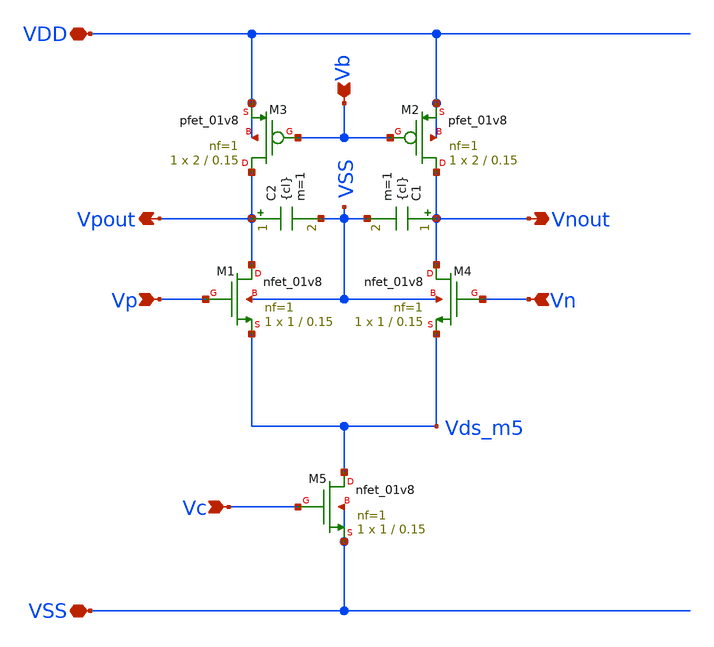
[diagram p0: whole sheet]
** sch_path: xschem/vco_stage_1.sch
**.subckt vco_stage_1 VDD VSS Vp Vn Vb Vc Vpout Vnout
*.iopin VDD
*.iopin VSS
*.ipin Vp
*.ipin Vn
*.ipin Vb
*.ipin Vc
*.opin Vpout
*.opin Vnout
XM1 Vpout Vp Vds_m5 VSS sky130_fd_pr__nfet_01v8 L=0.15 W=1 nf=1 ad='int((nf+1)/2) * W/nf * 0.29' as='int((nf+2)/2) * W/nf * 0.29'
+ pd='2*int((nf+1)/2) * (W/nf + 0.29)' ps='2*int((nf+2)/2) * (W/nf + 0.29)' nrd='0.29 / W' nrs='0.29 / W'
+ sa=0 sb=0 sd=0 mult=1 m=1
XM4 Vnout Vn Vds_m5 VSS sky130_fd_pr__nfet_01v8 L=0.15 W=1 nf=1 ad='int((nf+1)/2) * W/nf * 0.29' as='int((nf+2)/2) * W/nf * 0.29'
+ pd='2*int((nf+1)/2) * (W/nf + 0.29)' ps='2*int((nf+2)/2) * (W/nf + 0.29)' nrd='0.29 / W' nrs='0.29 / W'
+ sa=0 sb=0 sd=0 mult=1 m=1
XM5 Vds_m5 Vc VSS VSS sky130_fd_pr__nfet_01v8 L=0.15 W=1 nf=1 ad='int((nf+1)/2) * W/nf * 0.29' as='int((nf+2)/2) * W/nf * 0.29'
+ pd='2*int((nf+1)/2) * (W/nf + 0.29)' ps='2*int((nf+2)/2) * (W/nf + 0.29)' nrd='0.29 / W' nrs='0.29 / W'
+ sa=0 sb=0 sd=0 mult=1 m=1
XM2 Vnout Vb VDD VDD sky130_fd_pr__pfet_01v8 L=0.15 W=2 nf=1 ad='int((nf+1)/2) * W/nf * 0.29' as='int((nf+2)/2) * W/nf * 0.29'
+ pd='2*int((nf+1)/2) * (W/nf + 0.29)' ps='2*int((nf+2)/2) * (W/nf + 0.29)' nrd='0.29 / W' nrs='0.29 / W'
+ sa=0 sb=0 sd=0 mult=1 m=1
XM3 Vpout Vb VDD VDD sky130_fd_pr__pfet_01v8 L=0.15 W=2 nf=1 ad='int((nf+1)/2) * W/nf * 0.29' as='int((nf+2)/2) * W/nf * 0.29'
+ pd='2*int((nf+1)/2) * (W/nf + 0.29)' ps='2*int((nf+2)/2) * (W/nf + 0.29)' nrd='0.29 / W' nrs='0.29 / W'
+ sa=0 sb=0 sd=0 mult=1 m=1
C1 Vnout VSS {cl} m=1
C2 Vpout VSS {cl} m=1
**.ends
.end
